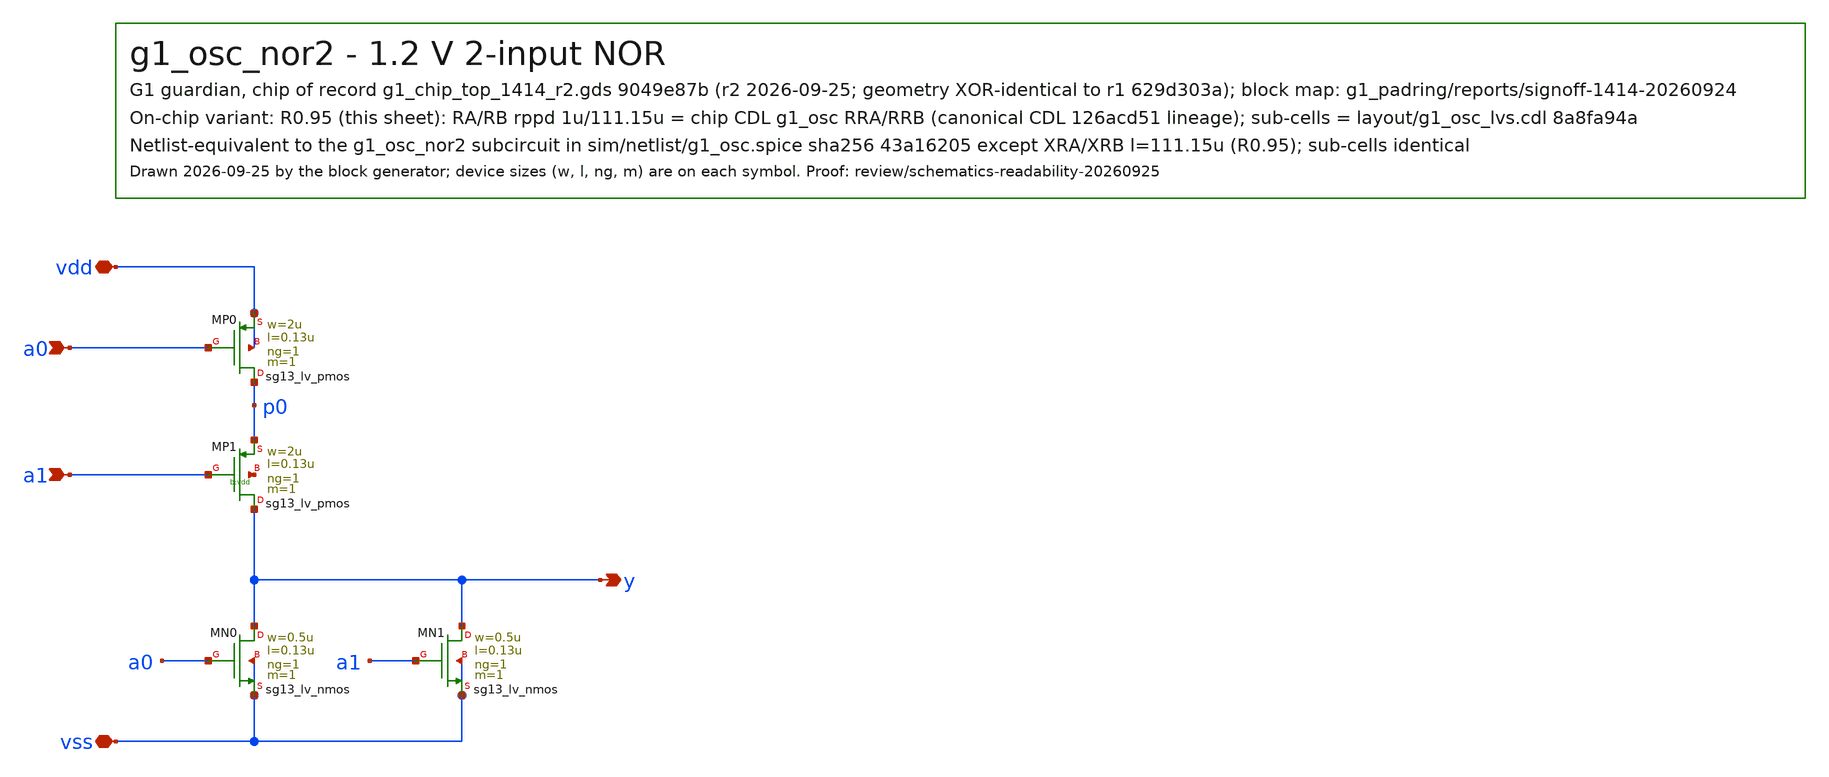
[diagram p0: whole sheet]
** sch_path: designs/g1-guardian/blocks/g1_osc/schematic/g1_osc_nor2.sch
**.subckt g1_osc_nor2 a0 a1 y vdd vss
*.ipin a0
*.ipin a1
*.opin y
*.iopin vdd
*.iopin vss
XMP0 p0 a0 vdd vdd sg13_lv_pmos w=2u l=0.13u ng=1 m=1 mm_ok=1
XMP1 y a1 p0 vdd sg13_lv_pmos w=2u l=0.13u ng=1 m=1 mm_ok=1
XMN0 y a0 vss vss sg13_lv_nmos w=0.5u l=0.13u ng=1 m=1 mm_ok=1
XMN1 y a1 vss vss sg13_lv_nmos w=0.5u l=0.13u ng=1 m=1 mm_ok=1
**.ends
.end
